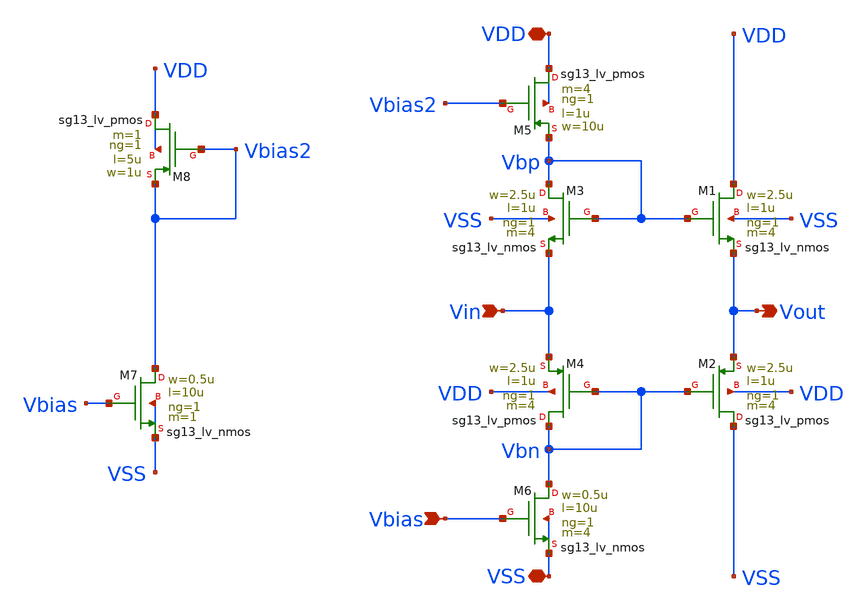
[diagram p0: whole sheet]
** sch_path: schema/ota_cmfb_core/ota_cmfb_core_output_stage.sch
**.subckt ota_cmfb_core_output_stage VSS VDD Vbias Vin Vout
*.iopin VSS
*.iopin VDD
*.ipin Vbias
*.ipin Vin
*.opin Vout
XM1 VDD Vbp Vout VSS sg13_lv_nmos w=2.5u l=1u ng=1 m=4 mm_ok=1
XM2 VSS Vbn Vout VDD sg13_lv_pmos w=2.5u l=1u ng=1 m=4 mm_ok=1
XM3 Vbp Vbp Vin VSS sg13_lv_nmos w=2.5u l=1u ng=1 m=4 mm_ok=1
XM4 Vbn Vbn Vin VDD sg13_lv_pmos w=2.5u l=1u ng=1 m=4 mm_ok=1
XM5 VDD Vbias2 Vbp VDD sg13_lv_pmos w=10u l=1u ng=1 m=4 mm_ok=1
XM6 Vbn Vbias VSS VSS sg13_lv_nmos w=0.5u l=10u ng=1 m=4 mm_ok=1
XM7 Vbias2 Vbias VSS VSS sg13_lv_nmos w=0.5u l=10u ng=1 m=1 mm_ok=1
XM8 VDD Vbias2 Vbias2 VDD sg13_lv_pmos w=1u l=5u ng=1 m=1 mm_ok=1
**.ends
.end
